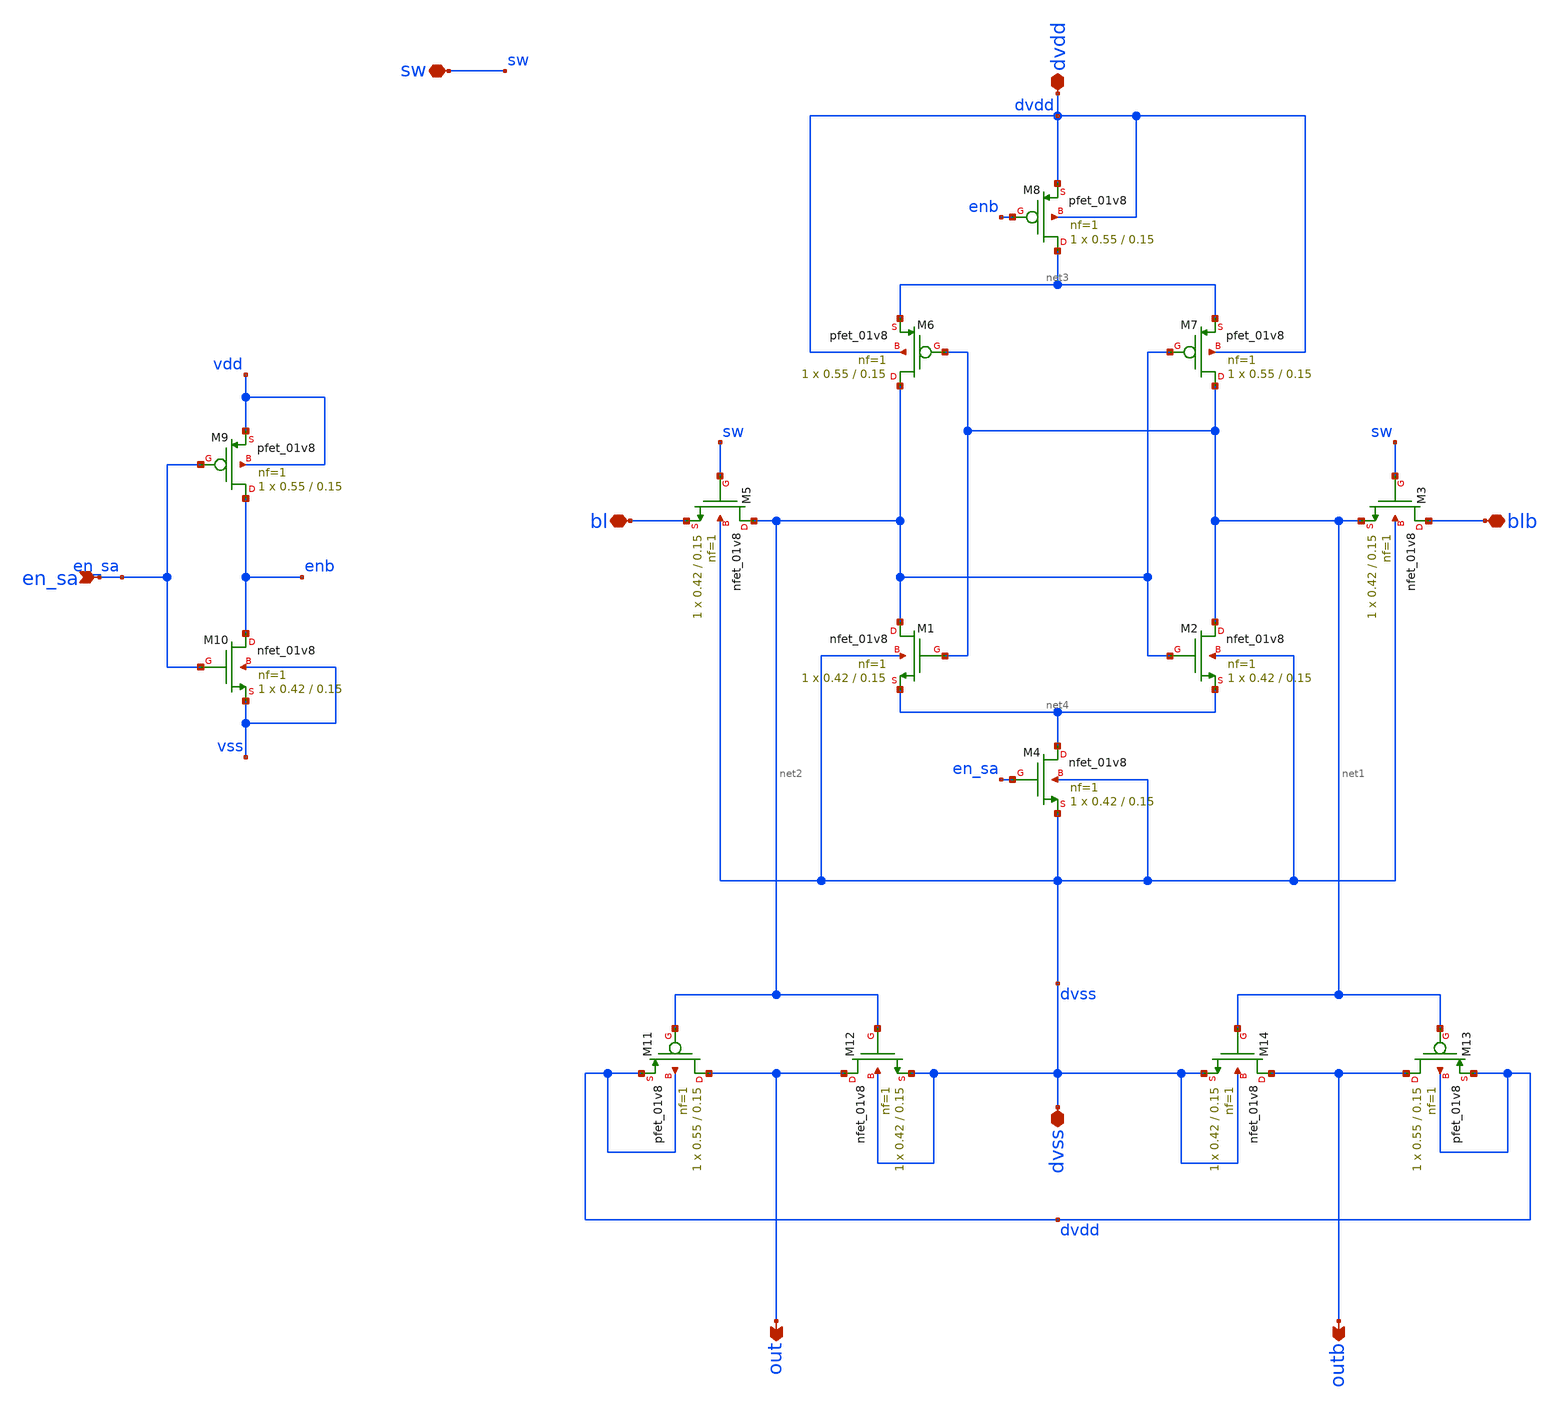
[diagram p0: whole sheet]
** sch_path: sense_amp.sch
**.subckt sense_amp blb dvss dvdd bl en_sa sw out outb
*.iopin blb
*.iopin dvss
*.iopin dvdd
*.iopin bl
*.ipin en_sa
*.iopin sw
*.opin out
*.opin outb
XM1 net2 net1 net4 dvss sky130_fd_pr__nfet_01v8 L=0.15 W=0.42 nf=1 ad='int((1 + 1)/2) * 0.42 / 1 * 0.29'
+ as='int((1 + 2)/2) * 0.42 / 1 * 0.29' pd='2*int((1 + 1)/2) * (0.42 / 1 + 0.29)' ps='2*int((1 + 2)/2) * (0.42 / 1 + 0.29)'
+ nrd='0.29 / 0.42 ' nrs='0.29 / 0.42 ' sa=0 sb=0 sd=0 mult=1 m=1
XM2 net1 net2 net4 dvss sky130_fd_pr__nfet_01v8 L=0.15 W=0.42 nf=1 ad='int((1 + 1)/2) * 0.42 / 1 * 0.29'
+ as='int((1 + 2)/2) * 0.42 / 1 * 0.29' pd='2*int((1 + 1)/2) * (0.42 / 1 + 0.29)' ps='2*int((1 + 2)/2) * (0.42 / 1 + 0.29)'
+ nrd='0.29 / 0.42 ' nrs='0.29 / 0.42 ' sa=0 sb=0 sd=0 mult=1 m=1
XM3 blb sw net1 dvss sky130_fd_pr__nfet_01v8 L=0.15 W=0.42 nf=1 ad='int((1 + 1)/2) * 0.42 / 1 * 0.29'
+ as='int((1 + 2)/2) * 0.42 / 1 * 0.29' pd='2*int((1 + 1)/2) * (0.42 / 1 + 0.29)' ps='2*int((1 + 2)/2) * (0.42 / 1 + 0.29)'
+ nrd='0.29 / 0.42 ' nrs='0.29 / 0.42 ' sa=0 sb=0 sd=0 mult=1 m=1
XM4 net4 en_sa dvss dvss sky130_fd_pr__nfet_01v8 L=0.15 W=0.42 nf=1 ad='int((1 + 1)/2) * 0.42 / 1 * 0.29'
+ as='int((1 + 2)/2) * 0.42 / 1 * 0.29' pd='2*int((1 + 1)/2) * (0.42 / 1 + 0.29)' ps='2*int((1 + 2)/2) * (0.42 / 1 + 0.29)'
+ nrd='0.29 / 0.42 ' nrs='0.29 / 0.42 ' sa=0 sb=0 sd=0 mult=1 m=1
XM5 net2 sw bl dvss sky130_fd_pr__nfet_01v8 L=0.15 W=0.42 nf=1 ad='int((1 + 1)/2) * 0.42 / 1 * 0.29'
+ as='int((1 + 2)/2) * 0.42 / 1 * 0.29' pd='2*int((1 + 1)/2) * (0.42 / 1 + 0.29)' ps='2*int((1 + 2)/2) * (0.42 / 1 + 0.29)'
+ nrd='0.29 / 0.42 ' nrs='0.29 / 0.42 ' sa=0 sb=0 sd=0 mult=1 m=1
XM6 net2 net1 net3 dvdd sky130_fd_pr__pfet_01v8 L=0.15 W=0.55 nf=1 ad='int((1 + 1)/2) * 0.55 / 1 * 0.29'
+ as='int((1 + 2)/2) * 0.55 / 1 * 0.29' pd='2*int((1 + 1)/2) * (0.55 / 1 + 0.29)' ps='2*int((1 + 2)/2) * (0.55 / 1 + 0.29)'
+ nrd='0.29 / 0.55 ' nrs='0.29 / 0.55 ' sa=0 sb=0 sd=0 mult=1 m=1
XM7 net1 net2 net3 dvdd sky130_fd_pr__pfet_01v8 L=0.15 W=0.55 nf=1 ad='int((1 + 1)/2) * 0.55 / 1 * 0.29'
+ as='int((1 + 2)/2) * 0.55 / 1 * 0.29' pd='2*int((1 + 1)/2) * (0.55 / 1 + 0.29)' ps='2*int((1 + 2)/2) * (0.55 / 1 + 0.29)'
+ nrd='0.29 / 0.55 ' nrs='0.29 / 0.55 ' sa=0 sb=0 sd=0 mult=1 m=1
XM8 net3 enb dvdd dvdd sky130_fd_pr__pfet_01v8 L=0.15 W=0.55 nf=1 ad='int((1 + 1)/2) * 0.55 / 1 * 0.29'
+ as='int((1 + 2)/2) * 0.55 / 1 * 0.29' pd='2*int((1 + 1)/2) * (0.55 / 1 + 0.29)' ps='2*int((1 + 2)/2) * (0.55 / 1 + 0.29)'
+ nrd='0.29 / 0.55 ' nrs='0.29 / 0.55 ' sa=0 sb=0 sd=0 mult=1 m=1
XM9 enb en_sa vdd vdd sky130_fd_pr__pfet_01v8 L=0.15 W=0.55 nf=1 ad='int((1 + 1)/2) * 0.55 / 1 * 0.29'
+ as='int((1 + 2)/2) * 0.55 / 1 * 0.29' pd='2*int((1 + 1)/2) * (0.55 / 1 + 0.29)' ps='2*int((1 + 2)/2) * (0.55 / 1 + 0.29)'
+ nrd='0.29 / 0.55 ' nrs='0.29 / 0.55 ' sa=0 sb=0 sd=0 mult=1 m=1
XM10 enb en_sa vss vss sky130_fd_pr__nfet_01v8 L=0.15 W=0.42 nf=1 ad='int((1 + 1)/2) * 0.42 / 1 * 0.29'
+ as='int((1 + 2)/2) * 0.42 / 1 * 0.29' pd='2*int((1 + 1)/2) * (0.42 / 1 + 0.29)' ps='2*int((1 + 2)/2) * (0.42 / 1 + 0.29)'
+ nrd='0.29 / 0.42 ' nrs='0.29 / 0.42 ' sa=0 sb=0 sd=0 mult=1 m=1
XM11 out net2 dvdd dvdd sky130_fd_pr__pfet_01v8 L=0.15 W=0.55 nf=1 ad='int((1 + 1)/2) * 0.55 / 1 * 0.29'
+ as='int((1 + 2)/2) * 0.55 / 1 * 0.29' pd='2*int((1 + 1)/2) * (0.55 / 1 + 0.29)' ps='2*int((1 + 2)/2) * (0.55 / 1 + 0.29)'
+ nrd='0.29 / 0.55 ' nrs='0.29 / 0.55 ' sa=0 sb=0 sd=0 mult=1 m=1
XM12 out net2 dvss dvss sky130_fd_pr__nfet_01v8 L=0.15 W=0.42 nf=1 ad='int((1 + 1)/2) * 0.42 / 1 * 0.29'
+ as='int((1 + 2)/2) * 0.42 / 1 * 0.29' pd='2*int((1 + 1)/2) * (0.42 / 1 + 0.29)' ps='2*int((1 + 2)/2) * (0.42 / 1 + 0.29)'
+ nrd='0.29 / 0.42 ' nrs='0.29 / 0.42 ' sa=0 sb=0 sd=0 mult=1 m=1
XM13 outb net1 dvdd dvdd sky130_fd_pr__pfet_01v8 L=0.15 W=0.55 nf=1 ad='int((1 + 1)/2) * 0.55 / 1 * 0.29'
+ as='int((1 + 2)/2) * 0.55 / 1 * 0.29' pd='2*int((1 + 1)/2) * (0.55 / 1 + 0.29)' ps='2*int((1 + 2)/2) * (0.55 / 1 + 0.29)'
+ nrd='0.29 / 0.55 ' nrs='0.29 / 0.55 ' sa=0 sb=0 sd=0 mult=1 m=1
XM14 outb net1 dvss dvss sky130_fd_pr__nfet_01v8 L=0.15 W=0.42 nf=1 ad='int((1 + 1)/2) * 0.42 / 1 * 0.29'
+ as='int((1 + 2)/2) * 0.42 / 1 * 0.29' pd='2*int((1 + 1)/2) * (0.42 / 1 + 0.29)' ps='2*int((1 + 2)/2) * (0.42 / 1 + 0.29)'
+ nrd='0.29 / 0.42 ' nrs='0.29 / 0.42 ' sa=0 sb=0 sd=0 mult=1 m=1
**.ends
.end
